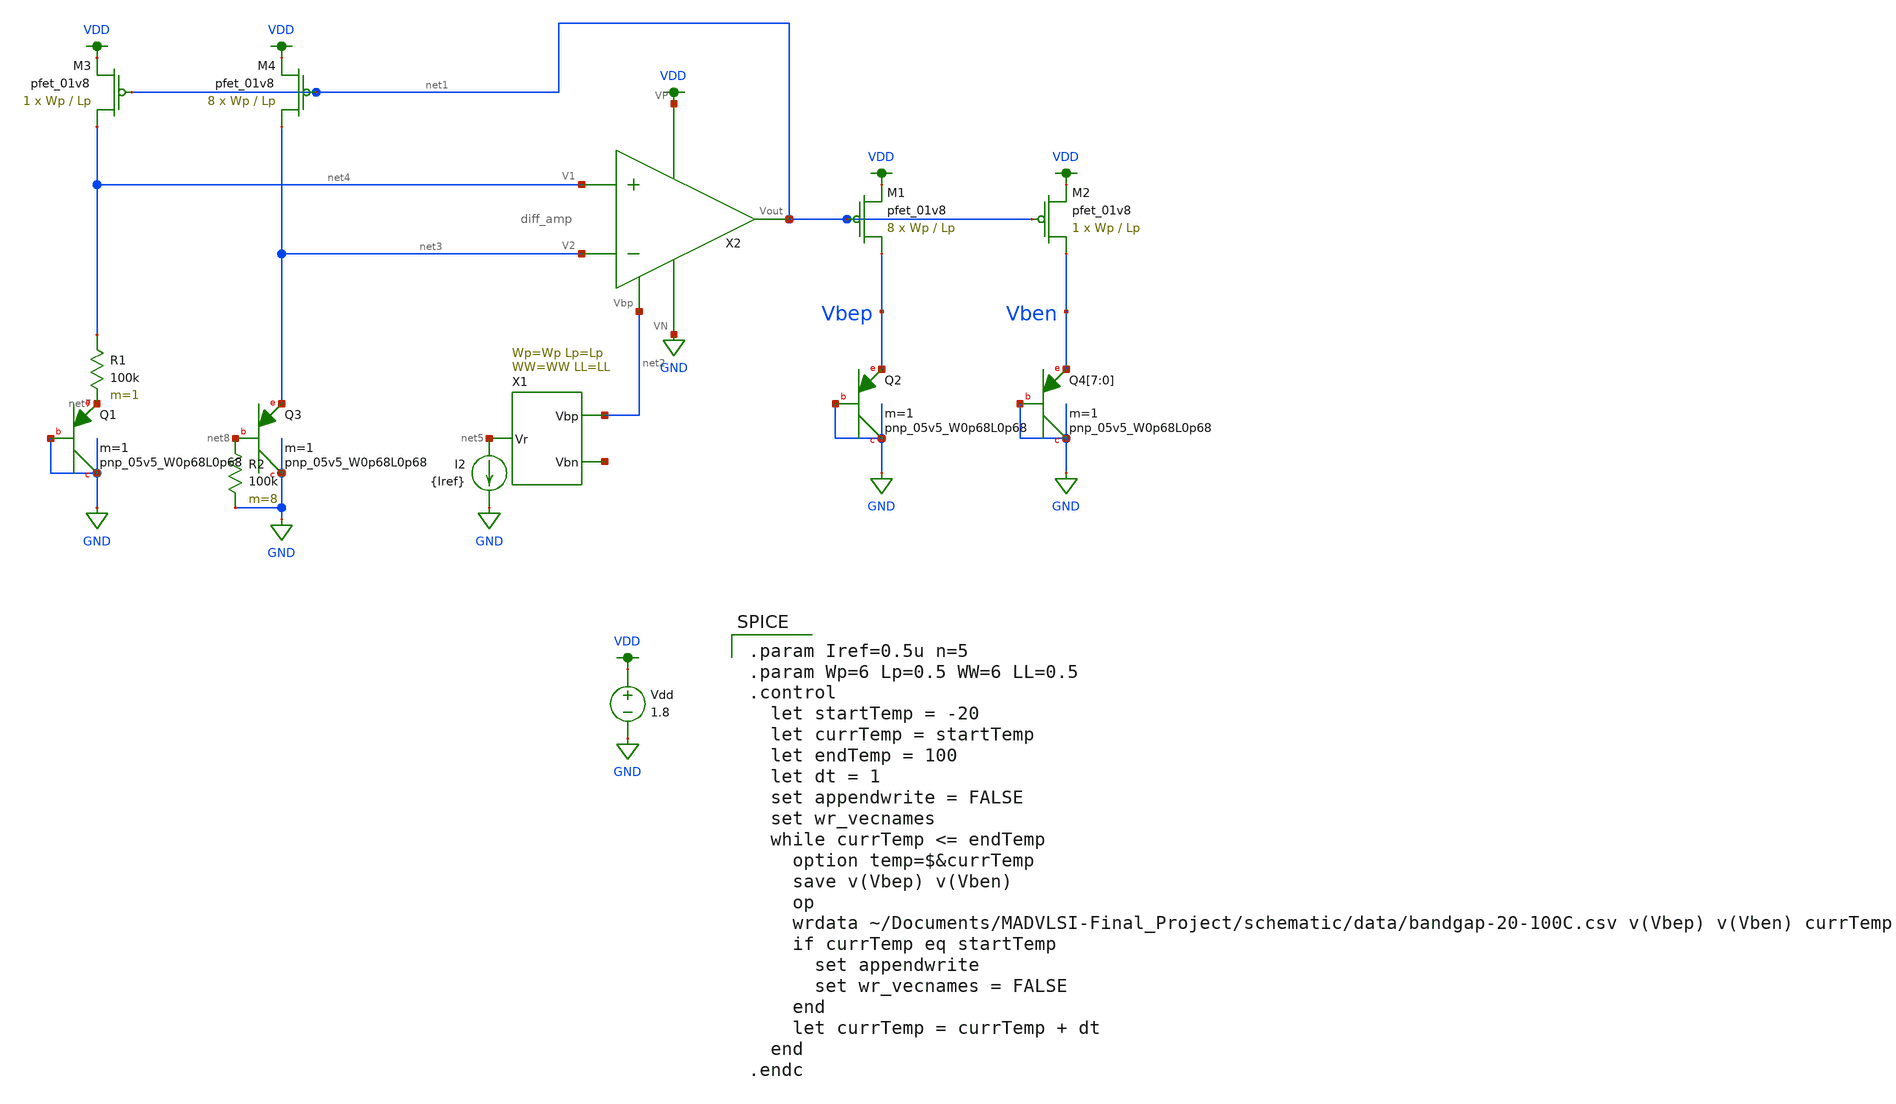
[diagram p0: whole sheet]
** sch_path: schematic/test/bandgap_test.sch
**.subckt bandgap_test
XQ2 GND GND Vbep sky130_fd_pr__pnp_05v5_W0p68L0p68 m=1
Vdd VDD GND 1.8
XM1 Vbep net1 VDD VDD sky130_fd_pr__pfet_01v8 L=Lp W=Wp nf=1 ad='int((nf+1)/2) * W/nf * 0.29' as='int((nf+2)/2) * W/nf * 0.29'
+ pd='2*int((nf+1)/2) * (W/nf + 0.29)' ps='2*int((nf+2)/2) * (W/nf + 0.29)' nrd='0.29 / W' nrs='0.29 / W'
+ sa=0 sb=0 sd=0 mult=8 m=8
XM2 Vben net1 VDD VDD sky130_fd_pr__pfet_01v8 L=Lp W=Wp nf=1 ad='int((nf+1)/2) * W/nf * 0.29' as='int((nf+2)/2) * W/nf * 0.29'
+ pd='2*int((nf+1)/2) * (W/nf + 0.29)' ps='2*int((nf+2)/2) * (W/nf + 0.29)' nrd='0.29 / W' nrs='0.29 / W'
+ sa=0 sb=0 sd=0 mult=1 m=1
X1 net5 net6 net2 ibias Wp=Wp Lp=Lp WW=WW LL=LL
I2 net5 GND {Iref}
XQ4[7] GND GND Vben sky130_fd_pr__pnp_05v5_W0p68L0p68 m=1
XQ4[6] GND GND Vben sky130_fd_pr__pnp_05v5_W0p68L0p68 m=1
XQ4[5] GND GND Vben sky130_fd_pr__pnp_05v5_W0p68L0p68 m=1
XQ4[4] GND GND Vben sky130_fd_pr__pnp_05v5_W0p68L0p68 m=1
XQ4[3] GND GND Vben sky130_fd_pr__pnp_05v5_W0p68L0p68 m=1
XQ4[2] GND GND Vben sky130_fd_pr__pnp_05v5_W0p68L0p68 m=1
XQ4[1] GND GND Vben sky130_fd_pr__pnp_05v5_W0p68L0p68 m=1
XQ4[0] GND GND Vben sky130_fd_pr__pnp_05v5_W0p68L0p68 m=1
X2 VDD net2 net1 net4 net3 GND diff_amp
XQ1 GND GND net7 sky130_fd_pr__pnp_05v5_W0p68L0p68 m=1
XQ3 GND net8 net3 sky130_fd_pr__pnp_05v5_W0p68L0p68 m=1
R1 net4 net7 100k m=1
R2 net8 GND 100k m=8
XM3 net4 net1 VDD VDD sky130_fd_pr__pfet_01v8 L=Lp W=Wp nf=1 ad='int((nf+1)/2) * W/nf * 0.29' as='int((nf+2)/2) * W/nf * 0.29'
+ pd='2*int((nf+1)/2) * (W/nf + 0.29)' ps='2*int((nf+2)/2) * (W/nf + 0.29)' nrd='0.29 / W' nrs='0.29 / W'
+ sa=0 sb=0 sd=0 mult=1 m=1
XM4 net3 net1 VDD VDD sky130_fd_pr__pfet_01v8 L=Lp W=Wp nf=1 ad='int((nf+1)/2) * W/nf * 0.29' as='int((nf+2)/2) * W/nf * 0.29'
+ pd='2*int((nf+1)/2) * (W/nf + 0.29)' ps='2*int((nf+2)/2) * (W/nf + 0.29)' nrd='0.29 / W' nrs='0.29 / W'
+ sa=0 sb=0 sd=0 mult=8 m=8
**** begin user architecture code

.option wnflag=1
.param MC_SWITCH=0.0
.lib ~/skywater/skywater-pdk/libraries/sky130_fd_pr_ngspice/latest/models/sky130.lib.spice tt


.param Iref=0.5u n=5
.param Wp=6 Lp=0.5 WW=6 LL=0.5
.control
  let startTemp = -20
  let currTemp = startTemp
  let endTemp = 100
  let dt = 1
  set appendwrite = FALSE
  set wr_vecnames
  while currTemp <= endTemp
    option temp=$&currTemp
    save v(Vbep) v(Vben)
    op
    wrdata ~/Documents/MADVLSI-Final_Project/schematic/data/bandgap-20-100C.csv v(Vbep) v(Vben)
+ currTemp
    if currTemp eq startTemp
      set appendwrite
      set wr_vecnames = FALSE
    end
    let currTemp = currTemp + dt
  end
.endc

**** end user architecture code
**.ends
.GLOBAL GND
.GLOBAL VDD
.end
